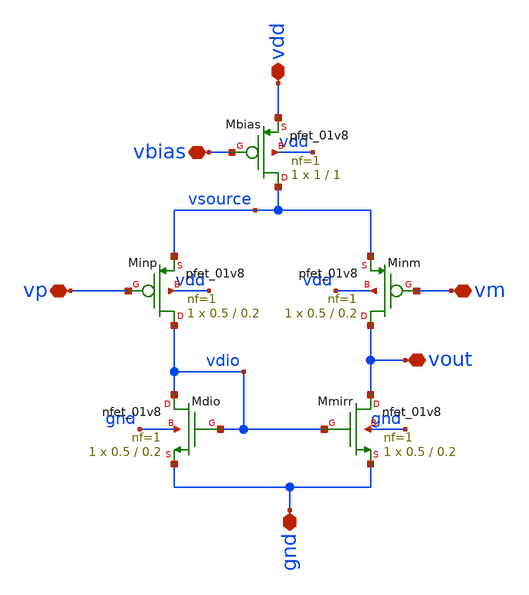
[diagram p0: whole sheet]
** sch_path: analog/xschem/final/col_amp_n_clamp_v1/amp_p_5T.sch
**.subckt amp_p_5T gnd vdd vout vm vp vbias
*.iopin gnd
*.iopin vdd
*.iopin vout
*.iopin vm
*.iopin vp
*.iopin vbias
XMinm vout vm vsource vdd sky130_fd_pr__pfet_01v8 L=0.2 W=0.5 nf=1 ad='int((1 + 1)/2) * 0.5 / 1 * 0.29'
+ as='int((1 + 2)/2) * 0.5 / 1 * 0.29' pd='2*int((1 + 1)/2) * (0.5 / 1 + 0.29)' ps='2*int((1 + 2)/2) * (0.5 / 1 + 0.29)'
+ nrd='0.29 / 0.5 ' nrs='0.29 / 0.5 ' sa=0 sb=0 sd=0 mult=1 m=1
XMinp vdio vp vsource vdd sky130_fd_pr__pfet_01v8 L=0.2 W=0.5 nf=1 ad='int((1 + 1)/2) * 0.5 / 1 * 0.29'
+ as='int((1 + 2)/2) * 0.5 / 1 * 0.29' pd='2*int((1 + 1)/2) * (0.5 / 1 + 0.29)' ps='2*int((1 + 2)/2) * (0.5 / 1 + 0.29)'
+ nrd='0.29 / 0.5 ' nrs='0.29 / 0.5 ' sa=0 sb=0 sd=0 mult=1 m=1
XMdio vdio vdio gnd gnd sky130_fd_pr__nfet_01v8 L=0.2 W=0.5 nf=1 ad='int((1 + 1)/2) * 0.5 / 1 * 0.29'
+ as='int((1 + 2)/2) * 0.5 / 1 * 0.29' pd='2*int((1 + 1)/2) * (0.5 / 1 + 0.29)' ps='2*int((1 + 2)/2) * (0.5 / 1 + 0.29)'
+ nrd='0.29 / 0.5 ' nrs='0.29 / 0.5 ' sa=0 sb=0 sd=0 mult=1 m=1
XMmirr vout vdio gnd gnd sky130_fd_pr__nfet_01v8 L=0.2 W=0.5 nf=1 ad='int((1 + 1)/2) * 0.5 / 1 * 0.29'
+ as='int((1 + 2)/2) * 0.5 / 1 * 0.29' pd='2*int((1 + 1)/2) * (0.5 / 1 + 0.29)' ps='2*int((1 + 2)/2) * (0.5 / 1 + 0.29)'
+ nrd='0.29 / 0.5 ' nrs='0.29 / 0.5 ' sa=0 sb=0 sd=0 mult=1 m=1
XMbias vsource vbias vdd vdd sky130_fd_pr__pfet_01v8 L=1 W=1 nf=1 ad='int((1 + 1)/2) * 1 / 1 * 0.29'
+ as='int((1 + 2)/2) * 1 / 1 * 0.29' pd='2*int((1 + 1)/2) * (1 / 1 + 0.29)' ps='2*int((1 + 2)/2) * (1 / 1 + 0.29)'
+ nrd='0.29 / 1 ' nrs='0.29 / 1 ' sa=0 sb=0 sd=0 mult=1 m=1
**.ends
.end
